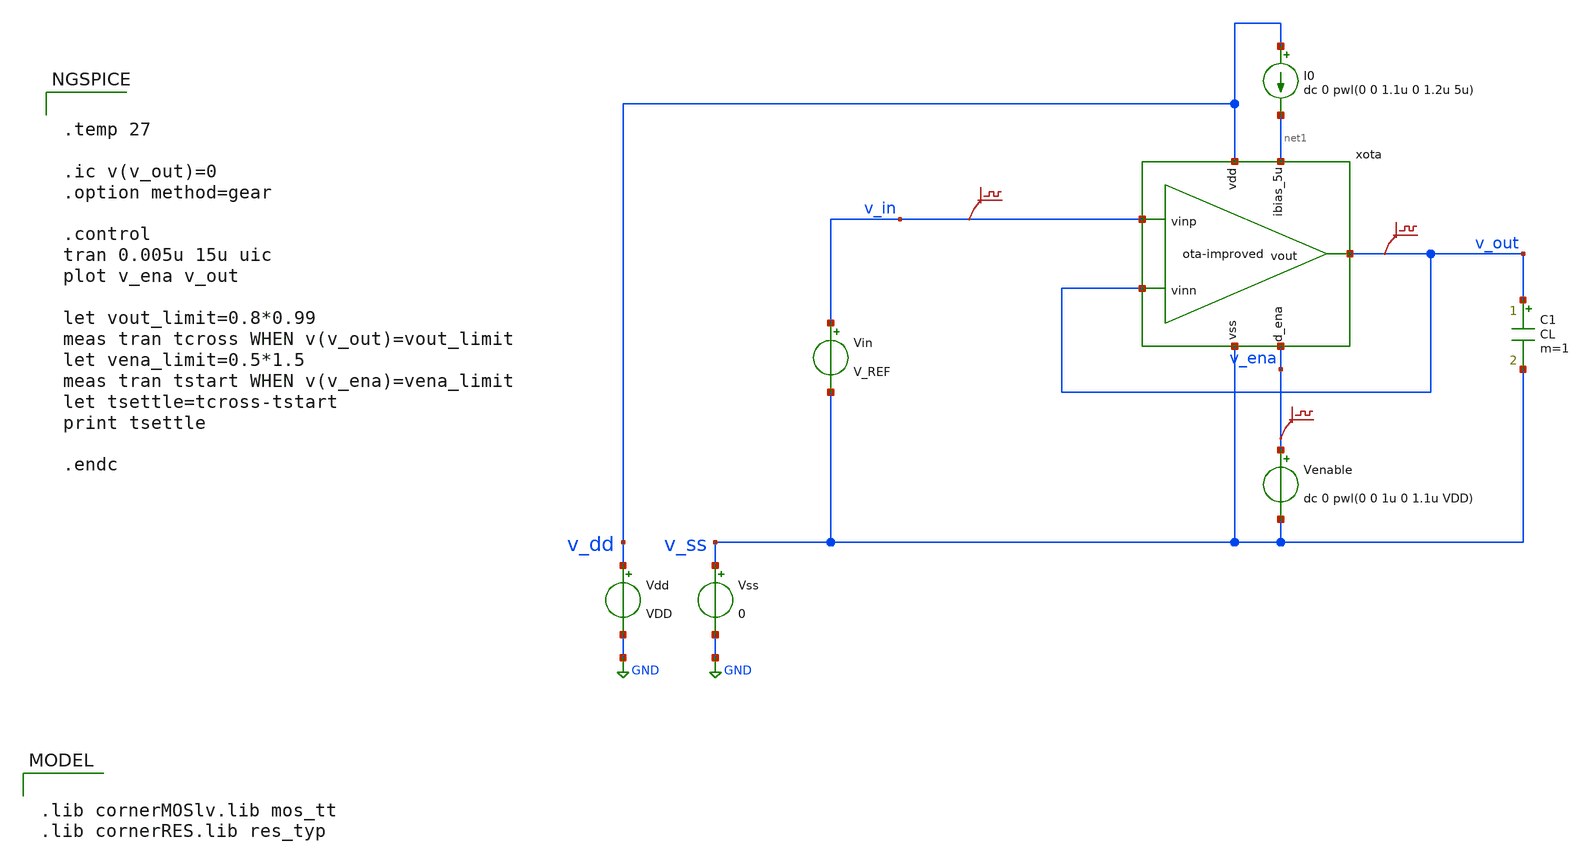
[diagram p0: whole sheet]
** sch_path: analog-db/circuits/amp_018_telescopic_cascode/pdk/ihp-sg13g2/schematic/ota-improved_tb-tran.sch
* (c) 2024-2025 Harald Pretl, Apache-2.0 license
**.subckt ota-improved_tb-tran
Vdd v_dd GND VDD
xota v_dd v_out v_in v_out net1 v_ena v_ss ota-improved
Vss v_ss GND 0
C1 v_out v_ss CL m=1
Vin v_in v_ss V_REF
I0 v_dd net1 dc 0 pwl(0 0 1.1u 0 1.2u 5u)
Venable v_ena v_ss dc 0 pwl(0 0 1u 0 1.1u VDD)
.save v(v_in)
.save v(v_out)
.save v(v_ena)
**** begin user architecture code


.temp 27

.ic v(v_out)=0
.option method=gear

.control
tran 0.005u 15u uic
plot v_ena v_out

let vout_limit=0.8*0.99
meas tran tcross WHEN v(v_out)=vout_limit
let vena_limit=0.5*1.5
meas tran tstart WHEN v(v_ena)=vena_limit
let tsettle=tcross-tstart
print tsettle

.endc



.lib cornerMOSlv.lib mos_tt
.lib cornerRES.lib res_typ




.param X_DUT_V_BIAS_1 = 0.6
.param X_DUT_V_BIAS_2 = 0.5

.param X_DUT_M5_L = 5u
.param X_DUT_M5_W = 6u
.param X_DUT_M5_NG = 3

.param X_DUT_M6_L = 5u
.param X_DUT_M6_W = 2u

.param X_DUT_M1M2_L = .5u
.param X_DUT_M1M2_W = 1u

.param X_DUT_M1CM2C_L = .5u
.param X_DUT_M1CM2C_W = 1u

.param X_DUT_M3CM4C_L = .5u
.param X_DUT_M3CM4C_W = 3u

.param X_DUT_M3M4_L = .5u
.param X_DUT_M3M4_W = 3u

.param VDD = 1.5
.param CL = 50f
.param V_CM = 0.8




**** end user architecture code
**.ends

* expanding   symbol:  ota-improved.sym # of pins=7
** sym_path: ota-improved.sym
** sch_path: ota-improved.sch
.subckt ota-improved vdd vout vinp vinn ibias_5u d_ena vss
*.ipin ibias_5u
*.iopin vdd
*.iopin vss
*.ipin vinp
*.ipin vinn
*.opin vout
*.ipin d_ena
XM5 net6 gate vss vss sg13_lv_nmos w=X_DUT_M5_W l=X_DUT_M5_L ng=X_DUT_M5_NG m=1 mm_ok=1
XM4 net2 gate_p vdd vdd sg13_lv_pmos w=X_DUT_M3M4_W l=X_DUT_M3M4_L ng=1 m=1 mm_ok=1
XM1 net4 vinp tail vss sg13_lv_nmos w=X_DUT_M1M2_W l=X_DUT_M1M2_L ng=1 m=1 mm_ok=1
XM2 net5 vinn tail vss sg13_lv_nmos w=X_DUT_M1M2_W l=X_DUT_M1M2_L ng=1 m=1 mm_ok=1
XM3 net3 gate_p vdd vdd sg13_lv_pmos w=X_DUT_M3M4_W l=X_DUT_M3M4_L ng=1 m=1 mm_ok=1
XM6 net1 gate vss vss sg13_lv_nmos w=X_DUT_M6_W l=X_DUT_M6_L ng=1 m=1 mm_ok=1
XMpd5 gate ena_n vss vss sg13_lv_nmos w=1u l=0.13u ng=1 m=1 mm_ok=1
XMpd3 ena ena_n vss vss sg13_lv_nmos w=1u l=0.13u ng=1 m=1 mm_ok=1
XMpd4 ena ena_n vdd vdd sg13_lv_pmos w=1u l=0.13u ng=1 m=1 mm_ok=1
XMpd6 net1 ena gate vss sg13_lv_nmos w=1u l=0.13u ng=1 m=1 mm_ok=1
XM2c vout dp_casc net5 vss sg13_lv_nmos w=X_DUT_M1CM2C_W l=X_DUT_M1CM2C_L ng=1 m=1 mm_ok=1
XM1c gate_p dp_casc net4 vss sg13_lv_nmos w=X_DUT_M1CM2C_W l=X_DUT_M1CM2C_L ng=1 m=1 mm_ok=1
XM4c vout gate_pc net2 vdd sg13_lv_pmos w=X_DUT_M3CM4C_W l=X_DUT_M3CM4C_L ng=1 m=1 mm_ok=1
XM3c gate_p gate_pc net3 vdd sg13_lv_pmos w=X_DUT_M3CM4C_W l=X_DUT_M3CM4C_L ng=1 m=1 mm_ok=1
XMpd8 gate_p ena vdd vdd sg13_lv_pmos w=1u l=0.13u ng=1 m=1 mm_ok=1
Vmeas1 tail net6 0
XMpd1 ena_n d_ena vss vss sg13_lv_nmos w=1u l=0.13u ng=1 m=1 mm_ok=1
XMpd2 ena_n d_ena vdd vdd sg13_lv_pmos w=1u l=0.13u ng=1 m=1 mm_ok=1
Vmeas4 ibias_5u net1 0
XMpd11 vout ena_n vss vss sg13_lv_nmos w=0.5u l=0.13u ng=1 m=1 mm_ok=1
XMdecoup1 vss gate vss vss sg13_lv_nmos w=8u l=1u ng=4 m=1 mm_ok=1
XMdecoup3 vdd gate_pc vdd vdd sg13_lv_pmos w=12u l=0.5u ng=4 m=1 mm_ok=1
V1 vdd gate_pc X_DUT_V_BIAS_2
V2 dp_casc tail X_DUT_V_BIAS_1
.ends

.GLOBAL GND
.end
